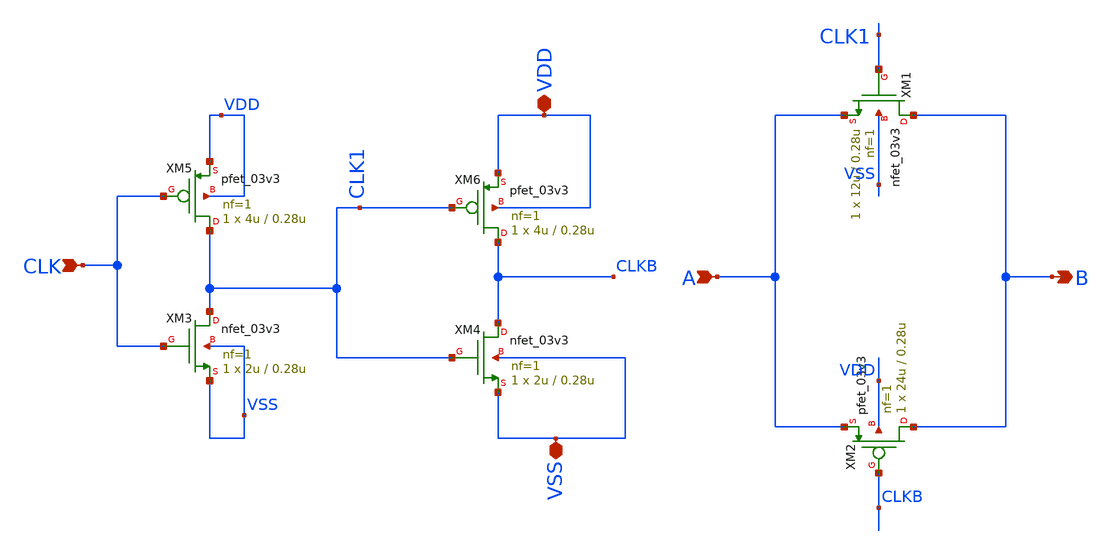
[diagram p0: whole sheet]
** sch_path: AWG_OUTPUT_AND_MUX_PAKISTAN_05/xschem/TG_GATE_SWITCH.sch
**.subckt TG_GATE_SWITCH VDD VSS B CLK A
*.iopin VDD
*.iopin VSS
*.opin B
*.ipin CLK
*.ipin A
XM4 CLKB CLK1 VSS VSS nfet_03v3 L=0.28u W=2u nf=1 ad='int((nf+1)/2) * W/nf * 0.18u' as='int((nf+2)/2) * W/nf * 0.18u'
+ pd='2*int((nf+1)/2) * (W/nf + 0.18u)' ps='2*int((nf+2)/2) * (W/nf + 0.18u)' nrd='0.18u / W' nrs='0.18u / W'
+ sa=0 sb=0 sd=0 m=1
XM6 CLKB CLK1 VDD VDD pfet_03v3 L=0.28u W=4u nf=1 ad='int((nf+1)/2) * W/nf * 0.18u' as='int((nf+2)/2) * W/nf * 0.18u'
+ pd='2*int((nf+1)/2) * (W/nf + 0.18u)' ps='2*int((nf+2)/2) * (W/nf + 0.18u)' nrd='0.18u / W' nrs='0.18u / W'
+ sa=0 sb=0 sd=0 m=1
XM1 B CLK1 A VSS nfet_03v3 L=0.28u W=12u nf=1 ad='int((nf+1)/2) * W/nf * 0.18u' as='int((nf+2)/2) * W/nf * 0.18u'
+ pd='2*int((nf+1)/2) * (W/nf + 0.18u)' ps='2*int((nf+2)/2) * (W/nf + 0.18u)' nrd='0.18u / W' nrs='0.18u / W'
+ sa=0 sb=0 sd=0 m=1
XM2 B CLKB A VDD pfet_03v3 L=0.28u W=24u nf=1 ad='int((nf+1)/2) * W/nf * 0.18u' as='int((nf+2)/2) * W/nf * 0.18u'
+ pd='2*int((nf+1)/2) * (W/nf + 0.18u)' ps='2*int((nf+2)/2) * (W/nf + 0.18u)' nrd='0.18u / W' nrs='0.18u / W'
+ sa=0 sb=0 sd=0 m=1
XM3 CLK1 CLK VSS VSS nfet_03v3 L=0.28u W=2u nf=1 ad='int((nf+1)/2) * W/nf * 0.18u' as='int((nf+2)/2) * W/nf * 0.18u'
+ pd='2*int((nf+1)/2) * (W/nf + 0.18u)' ps='2*int((nf+2)/2) * (W/nf + 0.18u)' nrd='0.18u / W' nrs='0.18u / W'
+ sa=0 sb=0 sd=0 m=1
XM5 CLK1 CLK VDD VDD pfet_03v3 L=0.28u W=4u nf=1 ad='int((nf+1)/2) * W/nf * 0.18u' as='int((nf+2)/2) * W/nf * 0.18u'
+ pd='2*int((nf+1)/2) * (W/nf + 0.18u)' ps='2*int((nf+2)/2) * (W/nf + 0.18u)' nrd='0.18u / W' nrs='0.18u / W'
+ sa=0 sb=0 sd=0 m=1
**.ends
.end
